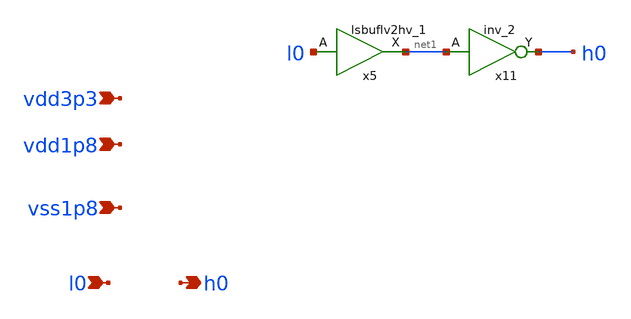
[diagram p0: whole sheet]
** sch_path: spice/xschem/array_1lsx.sch
**.subckt array_1lsx vdd1p8 vdd3p3 vss1p8 l0 h0
*.ipin vdd1p8
*.ipin vdd3p3
*.ipin vss1p8
*.ipin l0
*.opin h0
x5 l0 vdd1p8 vss1p8 vss1p8 vdd3p3 vdd3p3 net1 sky130_fd_sc_hvl__lsbuflv2hv_1
x11 net1 vss1p8 vss1p8 vdd3p3 vdd3p3 h0 sky130_fd_sc_hvl__inv_2
**.ends
.end
